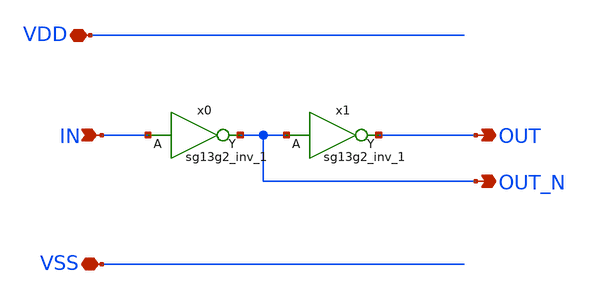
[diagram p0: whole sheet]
** sch_path: xschem/complementary_driver.sch
**.subckt complementary_driver VSS VDD IN OUT OUT_N
*.iopin VSS
*.iopin VDD
*.ipin IN
*.opin OUT
*.opin OUT_N
x0 OUT_N IN VDD VSS sg13g2_inv_1
x1 OUT OUT_N VDD VSS sg13g2_inv_1
**.ends

* expanding   symbol:  sg13g2_stdcells/sg13g2_inv_1.sym # of pins=2
** sym_path: sg13g2_stdcells/sg13g2_inv_1.sym
** sch_path: sg13g2_stdcells/sg13g2_inv_1.sch
.subckt sg13g2_inv_1 Y A VDD VSS
*.opin Y
*.ipin A
*.iopin VDD
*.iopin VSS
XM1 Y A VSS VSS sg13_lv_nmos w=740.00n l=130.00n ng=1 m=1 mm_ok=1
XM2 Y A VDD VDD sg13_lv_pmos w=1.12u l=130.00n ng=1 m=1 mm_ok=1
.ends

.end
